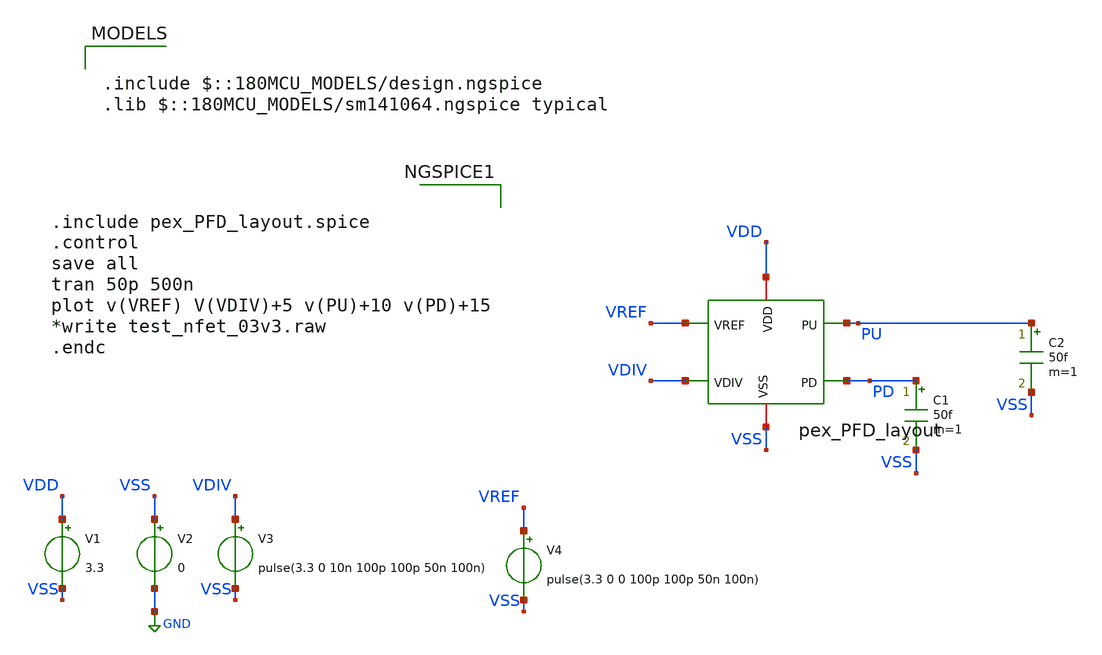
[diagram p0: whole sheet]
** sch_path: Clock_Generator_PAKISTAN_02/Schematics/pex_PFD_test.sch
**.subckt pex_PFD_test
V1 VDD VSS 3.3
V2 VSS GND 0
V3 VDIV VSS pulse(3.3 0 10n 100p 100p 50n 100n)
V4 VREF VSS pulse(3.3 0 0 100p 100p 50n 100n)
C1 PD VSS 50f m=1
C2 PU VSS 50f m=1
x1 VSS VREF VDIV PU PD VDD pex_PFD_layout
**** begin user architecture code

.include $::180MCU_MODELS/design.ngspice
.lib $::180MCU_MODELS/sm141064.ngspice typical



.include pex_PFD_layout.spice
.control
save all
tran 50p 500n
plot v(VREF) V(VDIV)+5 v(PU)+10 v(PD)+15
*write test_nfet_03v3.raw
.endc


**** end user architecture code
**.ends
.GLOBAL GND
.end
